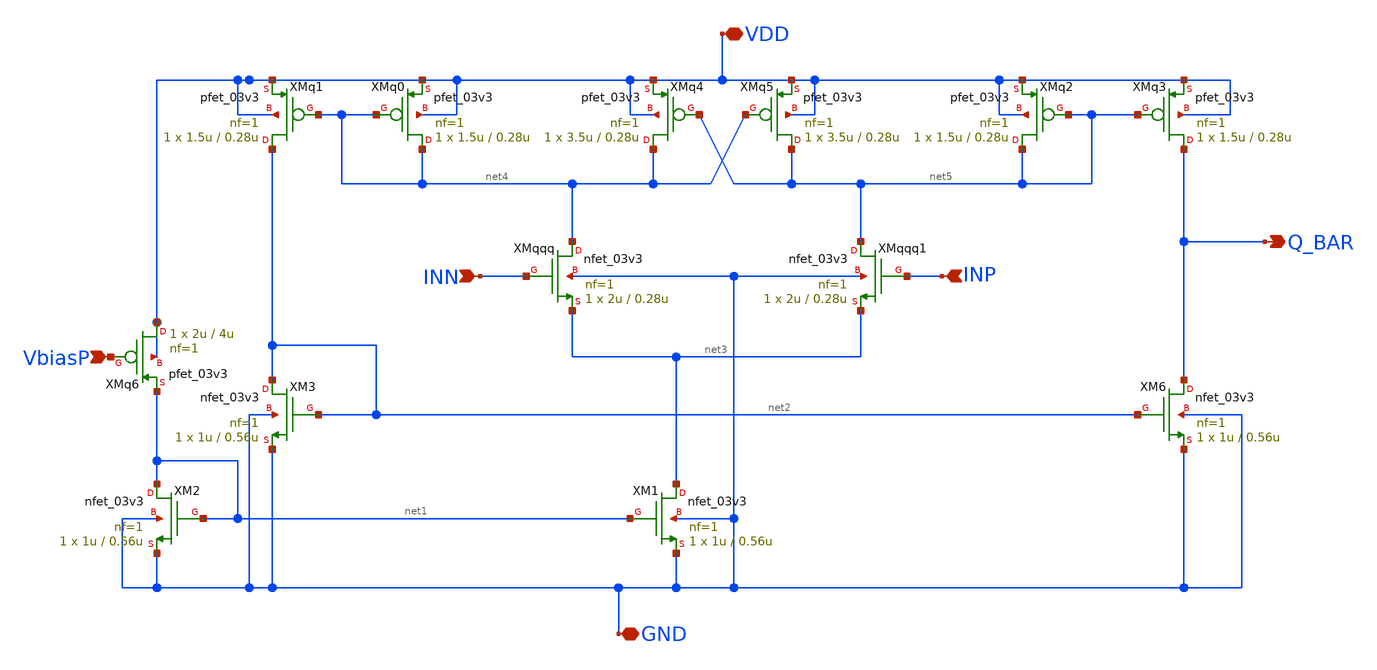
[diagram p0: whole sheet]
** sch_path: analog/B04_comparator.sch
**.subckt B04_comparator VDD GND INN INP Q_BAR VbiasP
*.iopin VDD
*.iopin GND
*.ipin INN
*.ipin INP
*.opin Q_BAR
*.ipin VbiasP
XM1 net3 net1 GND GND nfet_03v3 L=0.56u W=1u nf=1 ad='int((nf+1)/2) * W/nf * 0.18u' as='int((nf+2)/2) * W/nf * 0.18u'
+ pd='2*int((nf+1)/2) * (W/nf + 0.18u)' ps='2*int((nf+2)/2) * (W/nf + 0.18u)' nrd='0.18u / W' nrs='0.18u / W'
+ sa=0 sb=0 sd=0 m=1
XM2 net1 net1 GND GND nfet_03v3 L=0.56u W=1u nf=1 ad='int((nf+1)/2) * W/nf * 0.18u' as='int((nf+2)/2) * W/nf * 0.18u'
+ pd='2*int((nf+1)/2) * (W/nf + 0.18u)' ps='2*int((nf+2)/2) * (W/nf + 0.18u)' nrd='0.18u / W' nrs='0.18u / W'
+ sa=0 sb=0 sd=0 m=1
XM3 net2 net2 GND GND nfet_03v3 L=0.56u W=1u nf=1 ad='int((nf+1)/2) * W/nf * 0.18u' as='int((nf+2)/2) * W/nf * 0.18u'
+ pd='2*int((nf+1)/2) * (W/nf + 0.18u)' ps='2*int((nf+2)/2) * (W/nf + 0.18u)' nrd='0.18u / W' nrs='0.18u / W'
+ sa=0 sb=0 sd=0 m=1
XMqqq net4 INN net3 GND nfet_03v3 L=0.28u W=2u nf=1 ad='int((nf+1)/2) * W/nf * 0.18u' as='int((nf+2)/2) * W/nf * 0.18u'
+ pd='2*int((nf+1)/2) * (W/nf + 0.18u)' ps='2*int((nf+2)/2) * (W/nf + 0.18u)' nrd='0.18u / W' nrs='0.18u / W'
+ sa=0 sb=0 sd=0 m=1
XMqqq1 net5 INP net3 GND nfet_03v3 L=0.28u W=2u nf=1 ad='int((nf+1)/2) * W/nf * 0.18u' as='int((nf+2)/2) * W/nf * 0.18u'
+ pd='2*int((nf+1)/2) * (W/nf + 0.18u)' ps='2*int((nf+2)/2) * (W/nf + 0.18u)' nrd='0.18u / W' nrs='0.18u / W'
+ sa=0 sb=0 sd=0 m=1
XM6 Q_BAR net2 GND GND nfet_03v3 L=0.56u W=1u nf=1 ad='int((nf+1)/2) * W/nf * 0.18u' as='int((nf+2)/2) * W/nf * 0.18u'
+ pd='2*int((nf+1)/2) * (W/nf + 0.18u)' ps='2*int((nf+2)/2) * (W/nf + 0.18u)' nrd='0.18u / W' nrs='0.18u / W'
+ sa=0 sb=0 sd=0 m=1
XMq0 net4 net4 VDD VDD pfet_03v3 L=0.28u W=1.5u nf=1 ad='int((nf+1)/2) * W/nf * 0.18u' as='int((nf+2)/2) * W/nf * 0.18u'
+ pd='2*int((nf+1)/2) * (W/nf + 0.18u)' ps='2*int((nf+2)/2) * (W/nf + 0.18u)' nrd='0.18u / W' nrs='0.18u / W'
+ sa=0 sb=0 sd=0 m=1
XMq1 net2 net4 VDD VDD pfet_03v3 L=0.28u W=1.5u nf=1 ad='int((nf+1)/2) * W/nf * 0.18u' as='int((nf+2)/2) * W/nf * 0.18u'
+ pd='2*int((nf+1)/2) * (W/nf + 0.18u)' ps='2*int((nf+2)/2) * (W/nf + 0.18u)' nrd='0.18u / W' nrs='0.18u / W'
+ sa=0 sb=0 sd=0 m=1
XMq4 net4 net5 VDD VDD pfet_03v3 L=0.28u W=3.5u nf=1 ad='int((nf+1)/2) * W/nf * 0.18u' as='int((nf+2)/2) * W/nf * 0.18u'
+ pd='2*int((nf+1)/2) * (W/nf + 0.18u)' ps='2*int((nf+2)/2) * (W/nf + 0.18u)' nrd='0.18u / W' nrs='0.18u / W'
+ sa=0 sb=0 sd=0 m=1
XMq5 net5 net4 VDD VDD pfet_03v3 L=0.28u W=3.5u nf=1 ad='int((nf+1)/2) * W/nf * 0.18u' as='int((nf+2)/2) * W/nf * 0.18u'
+ pd='2*int((nf+1)/2) * (W/nf + 0.18u)' ps='2*int((nf+2)/2) * (W/nf + 0.18u)' nrd='0.18u / W' nrs='0.18u / W'
+ sa=0 sb=0 sd=0 m=1
XMq2 net5 net5 VDD VDD pfet_03v3 L=0.28u W=1.5u nf=1 ad='int((nf+1)/2) * W/nf * 0.18u' as='int((nf+2)/2) * W/nf * 0.18u'
+ pd='2*int((nf+1)/2) * (W/nf + 0.18u)' ps='2*int((nf+2)/2) * (W/nf + 0.18u)' nrd='0.18u / W' nrs='0.18u / W'
+ sa=0 sb=0 sd=0 m=1
XMq3 Q_BAR net5 VDD VDD pfet_03v3 L=0.28u W=1.5u nf=1 ad='int((nf+1)/2) * W/nf * 0.18u' as='int((nf+2)/2) * W/nf * 0.18u'
+ pd='2*int((nf+1)/2) * (W/nf + 0.18u)' ps='2*int((nf+2)/2) * (W/nf + 0.18u)' nrd='0.18u / W' nrs='0.18u / W'
+ sa=0 sb=0 sd=0 m=1
XMq6 VDD VbiasP net1 VDD pfet_03v3 L=4u W=2u nf=1 ad='int((nf+1)/2) * W/nf * 0.18u' as='int((nf+2)/2) * W/nf * 0.18u'
+ pd='2*int((nf+1)/2) * (W/nf + 0.18u)' ps='2*int((nf+2)/2) * (W/nf + 0.18u)' nrd='0.18u / W' nrs='0.18u / W'
+ sa=0 sb=0 sd=0 m=1
**.ends
.end
